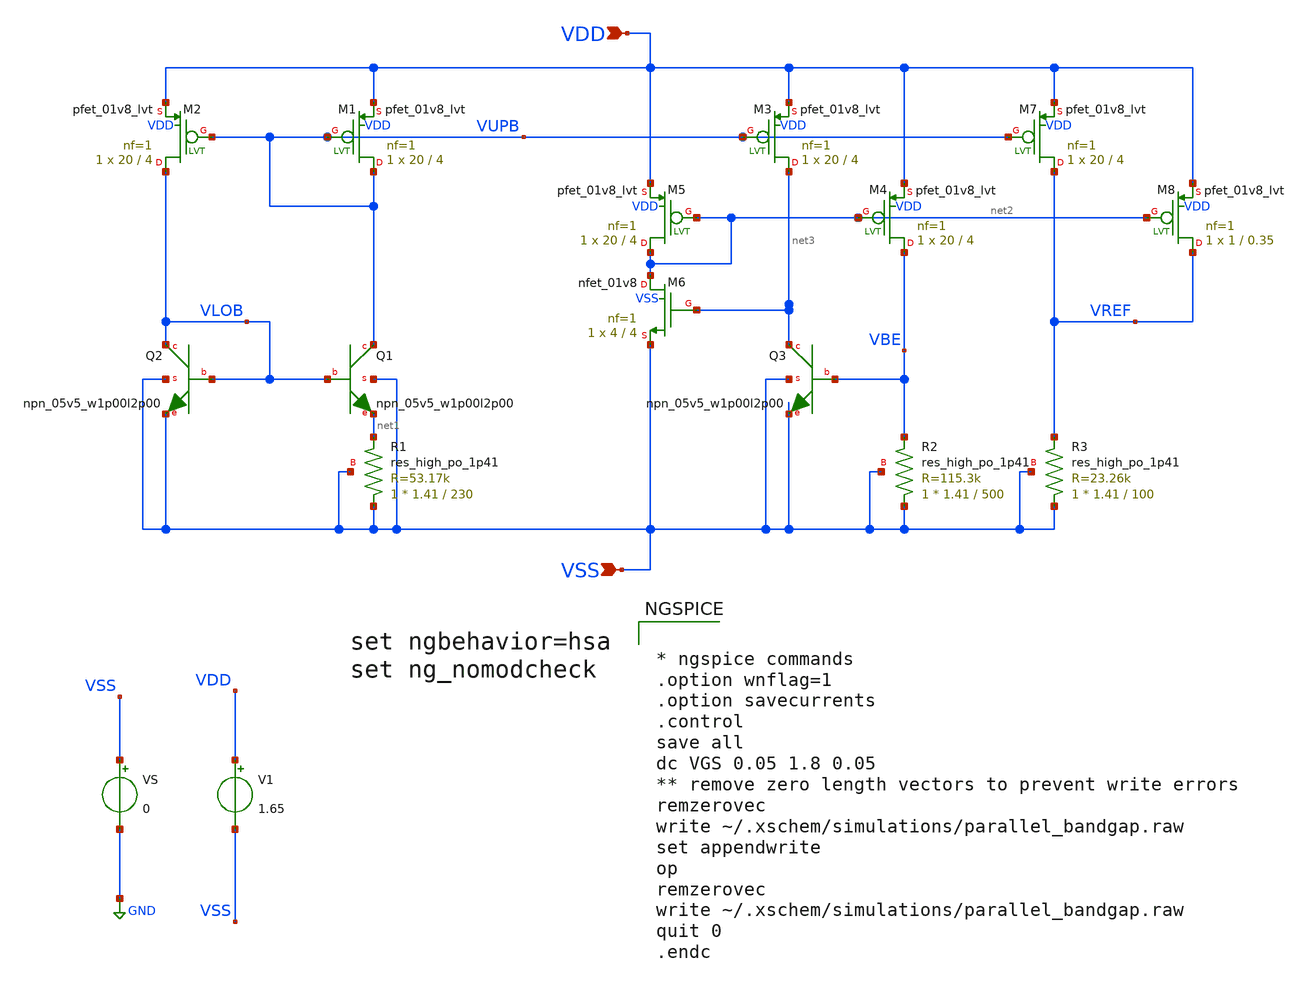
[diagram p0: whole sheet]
** sch_path: designs/parallel_bandgap.sch
**.subckt parallel_bandgap VDD VSS
*.ipin VDD
*.ipin VSS
XM1 VUPB VUPB VDD VDD sky130_fd_pr__pfet_01v8_lvt L=4 W=20 nf=1 ad='int((nf+1)/2) * W/nf * 0.29' as='int((nf+2)/2) * W/nf * 0.29'
+ pd='2*int((nf+1)/2) * (W/nf + 0.29)' ps='2*int((nf+2)/2) * (W/nf + 0.29)' nrd='0.29 / W' nrs='0.29 / W'
+ sa=0 sb=0 sd=0 mult=1 m=1
XM2 VLOB VUPB VDD VDD sky130_fd_pr__pfet_01v8_lvt L=4 W=20 nf=1 ad='int((nf+1)/2) * W/nf * 0.29' as='int((nf+2)/2) * W/nf * 0.29'
+ pd='2*int((nf+1)/2) * (W/nf + 0.29)' ps='2*int((nf+2)/2) * (W/nf + 0.29)' nrd='0.29 / W' nrs='0.29 / W'
+ sa=0 sb=0 sd=0 mult=1 m=1
XQ1 VUPB VLOB net1 VSS sky130_fd_pr__npn_05v5_w1p00l2p00
XQ2 VLOB VLOB VSS VSS sky130_fd_pr__npn_05v5_w1p00l2p00
XR1 VSS net1 VSS sky130_fd_pr__res_high_po_1p41 L=230 mult=1 m=1
XM3 net3 VUPB VDD VDD sky130_fd_pr__pfet_01v8_lvt L=4 W=20 nf=1 ad='int((nf+1)/2) * W/nf * 0.29' as='int((nf+2)/2) * W/nf * 0.29'
+ pd='2*int((nf+1)/2) * (W/nf + 0.29)' ps='2*int((nf+2)/2) * (W/nf + 0.29)' nrd='0.29 / W' nrs='0.29 / W'
+ sa=0 sb=0 sd=0 mult=1 m=1
XQ3 net3 VBE VSS VSS sky130_fd_pr__npn_05v5_w1p00l2p00
XR2 VSS VBE VSS sky130_fd_pr__res_high_po_1p41 L=500 mult=1 m=1
XM4 VBE net2 VDD VDD sky130_fd_pr__pfet_01v8_lvt L=4 W=20 nf=1 ad='int((nf+1)/2) * W/nf * 0.29' as='int((nf+2)/2) * W/nf * 0.29'
+ pd='2*int((nf+1)/2) * (W/nf + 0.29)' ps='2*int((nf+2)/2) * (W/nf + 0.29)' nrd='0.29 / W' nrs='0.29 / W'
+ sa=0 sb=0 sd=0 mult=1 m=1
XM5 net2 net2 VDD VDD sky130_fd_pr__pfet_01v8_lvt L=4 W=20 nf=1 ad='int((nf+1)/2) * W/nf * 0.29' as='int((nf+2)/2) * W/nf * 0.29'
+ pd='2*int((nf+1)/2) * (W/nf + 0.29)' ps='2*int((nf+2)/2) * (W/nf + 0.29)' nrd='0.29 / W' nrs='0.29 / W'
+ sa=0 sb=0 sd=0 mult=1 m=1
XM6 net2 net3 VSS VSS sky130_fd_pr__nfet_01v8 L=4 W=4 nf=1 ad='int((nf+1)/2) * W/nf * 0.29' as='int((nf+2)/2) * W/nf * 0.29'
+ pd='2*int((nf+1)/2) * (W/nf + 0.29)' ps='2*int((nf+2)/2) * (W/nf + 0.29)' nrd='0.29 / W' nrs='0.29 / W'
+ sa=0 sb=0 sd=0 mult=1 m=1
XM7 VREF VUPB VDD VDD sky130_fd_pr__pfet_01v8_lvt L=4 W=20 nf=1 ad='int((nf+1)/2) * W/nf * 0.29' as='int((nf+2)/2) * W/nf * 0.29'
+ pd='2*int((nf+1)/2) * (W/nf + 0.29)' ps='2*int((nf+2)/2) * (W/nf + 0.29)' nrd='0.29 / W' nrs='0.29 / W'
+ sa=0 sb=0 sd=0 mult=1 m=1
XR3 VSS VREF VSS sky130_fd_pr__res_high_po_1p41 L=100 mult=1 m=1
XM8 VREF net2 VDD VDD sky130_fd_pr__pfet_01v8_lvt L=0.35 W=1 nf=1 ad='int((nf+1)/2) * W/nf * 0.29' as='int((nf+2)/2) * W/nf * 0.29'
+ pd='2*int((nf+1)/2) * (W/nf + 0.29)' ps='2*int((nf+2)/2) * (W/nf + 0.29)' nrd='0.29 / W' nrs='0.29 / W'
+ sa=0 sb=0 sd=0 mult=1 m=1
V1 VDD VSS 1.65
.save i(v1)
VS VSS GND 0
**** begin user architecture code


* ngspice commands
.option wnflag=1
.option savecurrents
.control
save all
dc VGS 0.05 1.8 0.05
** remove zero length vectors to prevent write errors
remzerovec
write ~/.xschem/simulations/parallel_bandgap.raw
set appendwrite
op
remzerovec
write ~/.xschem/simulations/parallel_bandgap.raw
quit 0
.endc



** opencircuitdesign pdks install
.lib $::SKYWATER_MODELS/sky130.lib.spice ss


**** end user architecture code
**.ends
.GLOBAL GND
.end
